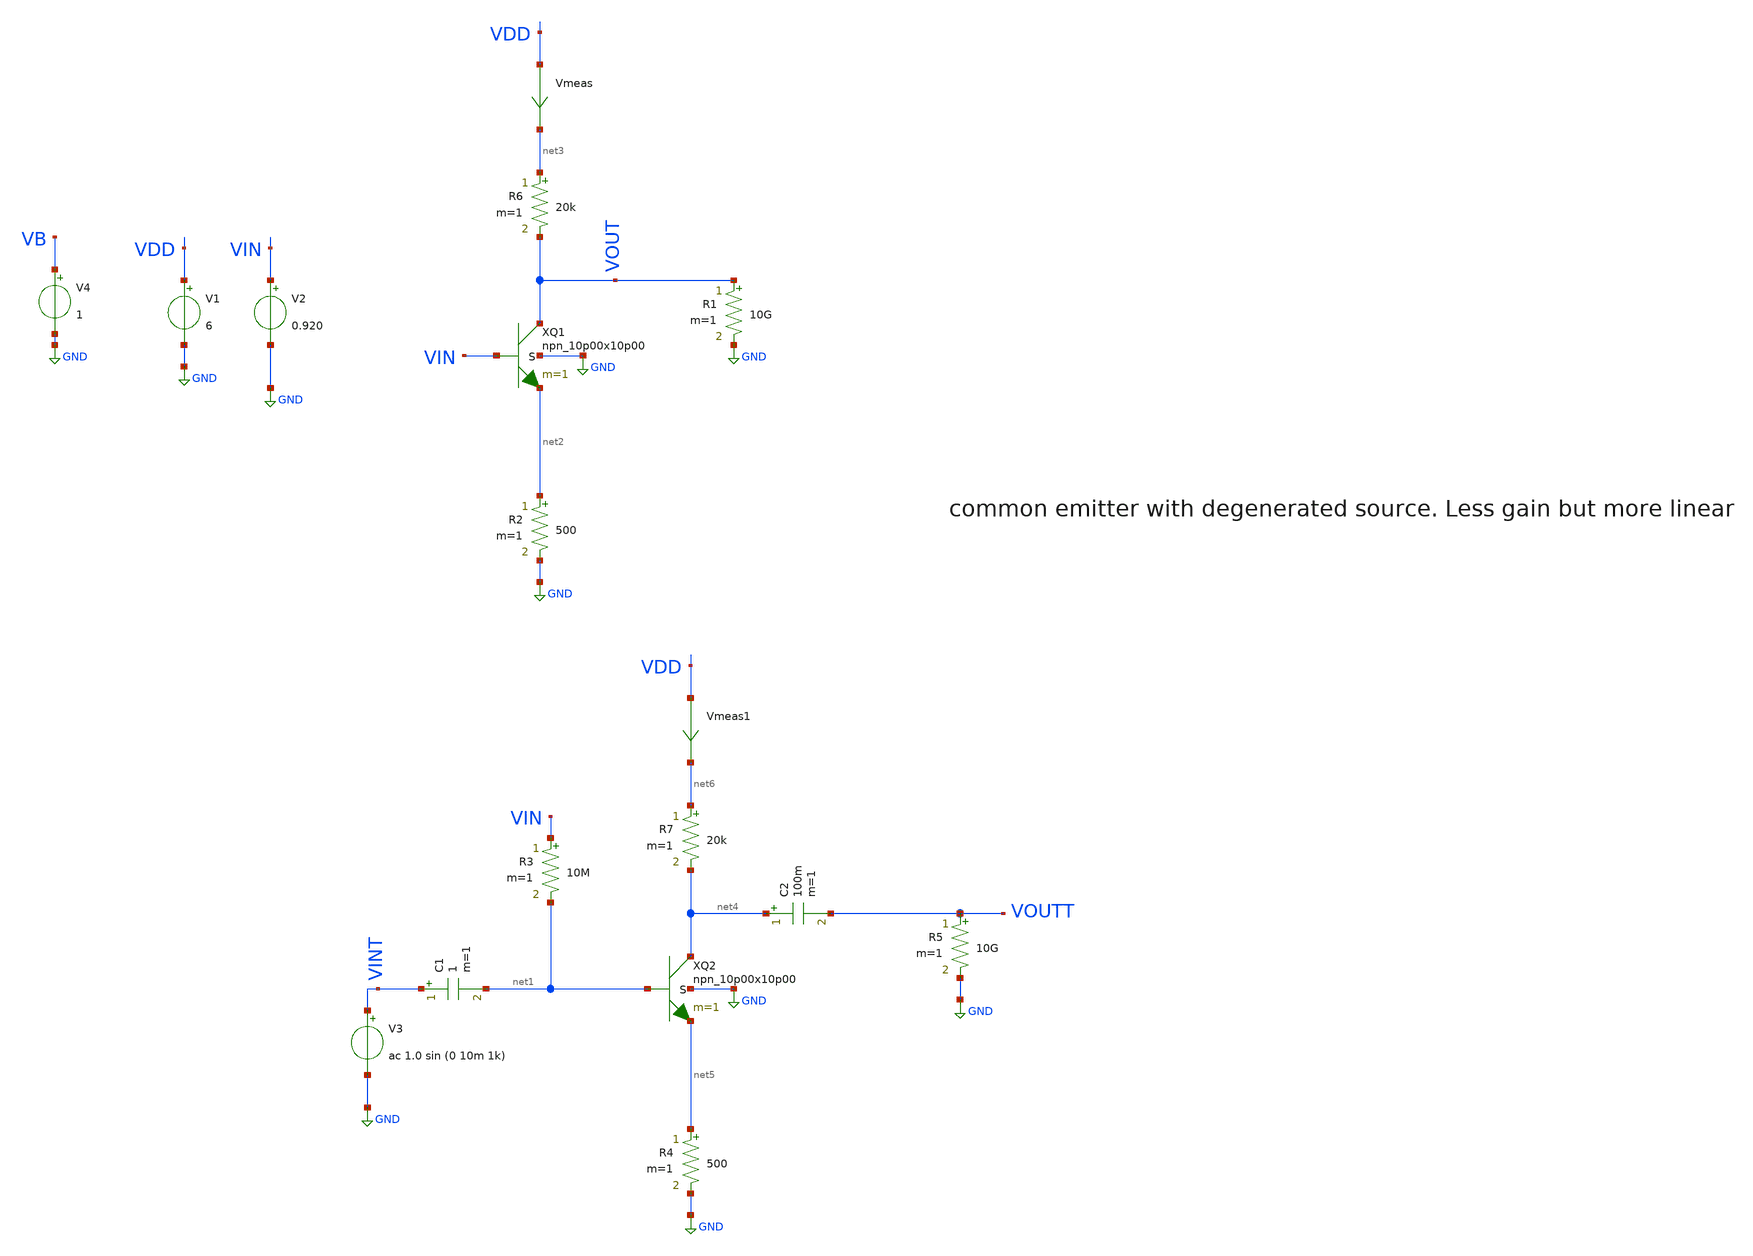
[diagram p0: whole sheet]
** sch_path: basic_circuits/bipolar_stage_emitter_degenerated.sch
**.subckt bipolar_stage_emitter_degenerated
Vmeas VDD net3 0
.save i(vmeas)
V1 VDD GND 6
V2 VIN GND 0.920
V3 VINT GND ac 1.0 sin (0 10m 1k)
R3 VIN net1 10M m=1
R5 VOUTT GND 10G m=1
V4 VB GND 1
R1 VOUT GND 10G m=1
C1 VINT net1 1 m=1
XQ1 VOUT VIN net2 GND npn_10p00x10p00 m=1
C2 net4 VOUTT 100m m=1
R6 net3 VOUT 20k m=1
Vmeas1 VDD net6 0
.save i(vmeas1)
R4 net5 GND 500 m=1
XQ2 net4 net1 net5 GND npn_10p00x10p00 m=1
R7 net6 net4 20k m=1
R2 net2 GND 500 m=1
**** begin user architecture code

**************************************************************
**************************************************************
**************************************************************
**************************************************************
**************************************************************
*LIBs*********************************************************
**************************************************************
**************************************************************
**************************************************************
**************************************************************
**************************************************************
.include $::180MCU_MODELS/design.ngspice
*.lib $::180MCU_MODELS/sm141064.ngspice statistical *use statistical if you want global and parameter mismatch
*.lib $::180MCU_MODELS/sm141064.ngspice res_statistical
.lib $::180MCU_MODELS/sm141064.ngspice typical
.lib $::180MCU_MODELS/sm141064.ngspice res_typical
.lib $::180MCU_MODELS/sm141064.ngspice moscap_typical
.lib $::180MCU_MODELS/sm141064.ngspice bjt_typical
.lib $::180MCU_MODELS/sm141064.ngspice diode_typical
.lib $::180MCU_MODELS/sm141064.ngspice mimcap_typical
**************************************************************
**************************************************************
**************************************************************
**************************************************************
**************************************************************
*Corners/montecarlo options***********************************
**************************************************************
**************************************************************
**************************************************************
**************************************************************
**************************************************************
.TEMP 27
.param   sw_stat_global = 1   sw_stat_mism = 1  mc_skew = 3  res_mc_skew = 3  cap_mc_skew = 3
+  fnoicor = 1
**************************************************************
**************************************************************
**************************************************************
**************************************************************
*SIMULATION and Plots*****************************************
**************************************************************
**************************************************************
**************************************************************
**************************************************************
.control
save all
dc V2 0 6 0.01
*dc simulation
plot v(VOUT) v(VIN) deriv(v(VOUT))
*ploting VIN VOUT and the voltage gain
plot i(Vmeas)
*ploting the current for curiosity
tran 100ns 2m
*transient simulation
plot (v(VINT)) (v(VOUTT))
*simple plot to exemplify the gain
fft v(VOUTT) v(VINT)
*fast fourier transfor
plot mag(v(VOUTT)) mag(v(VINT))
* analyse the frequency spectrum of the transient waves, to detect distortion
ac dec 20 1 50G
*simple ac simulation
plot v(VOUTT)
*gain in function of the input frequency
.endc

**** end user architecture code
**.ends
.GLOBAL GND
.end
